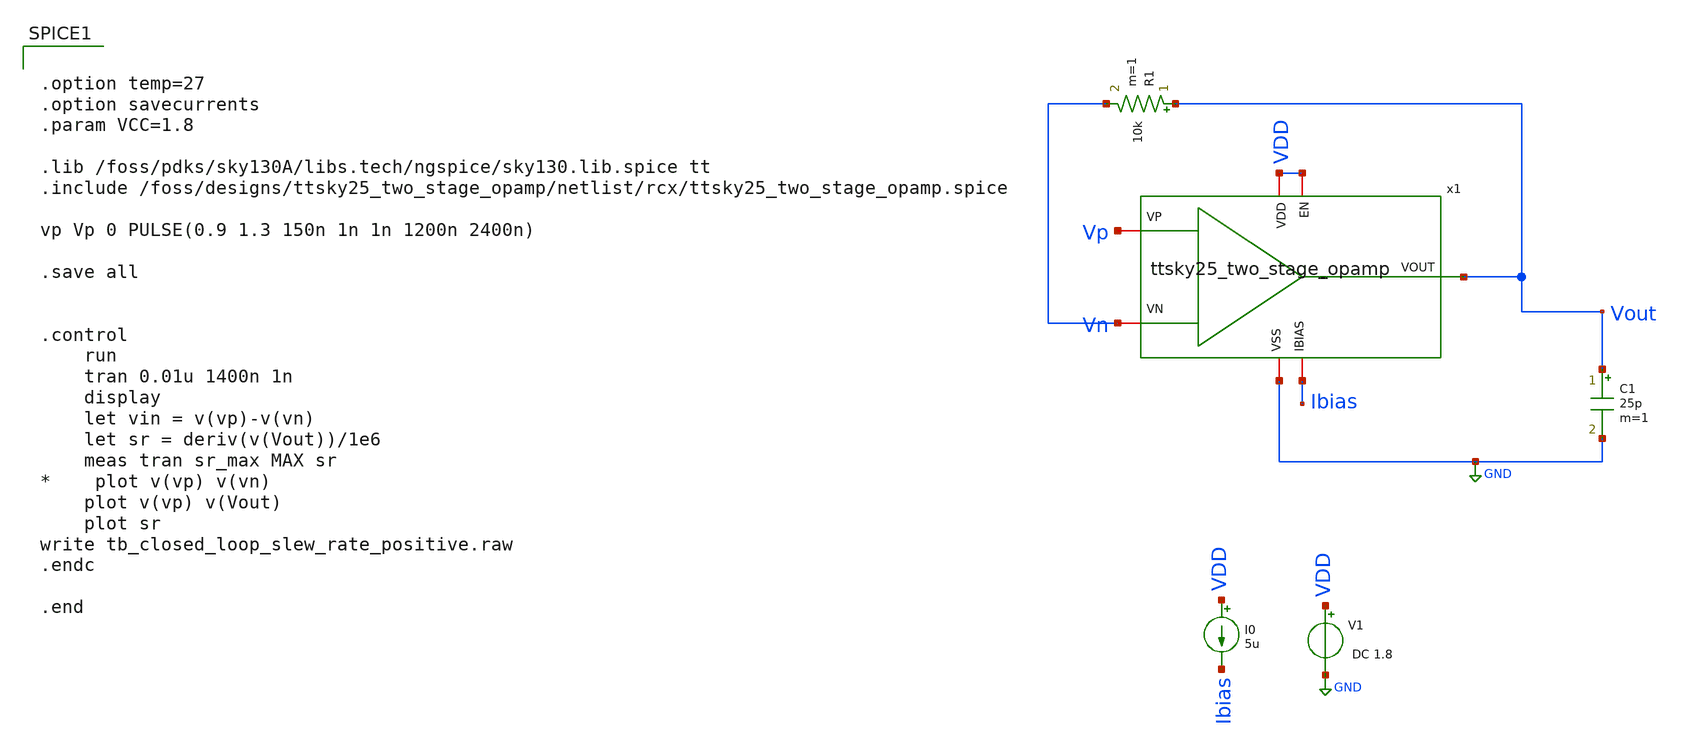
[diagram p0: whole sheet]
** sch_path: xschem/post-layout/testbenches/tb_closed_loop_slew_rate_positive.sch
**.subckt tb_closed_loop_slew_rate_positive
V1 VDD GND DC 1.8
I0 VDD Ibias 5u
C1 Vout GND 25p m=1
R1 Vout Vn 10k m=1
x1 VDD Ibias Vout Vn Vp VDD GND ttsky25_two_stage_opamp
**** begin user architecture code


.option temp=27
.option savecurrents
.param VCC=1.8

.lib /foss/pdks/sky130A/libs.tech/ngspice/sky130.lib.spice tt
.include /foss/designs/ttsky25_two_stage_opamp/netlist/rcx/ttsky25_two_stage_opamp.spice

vp Vp 0 PULSE(0.9 1.3 150n 1n 1n 1200n 2400n)

.save all


.control
	run
	tran 0.01u 1400n 1n
	display
	let vin = v(vp)-v(vn)
	let sr = deriv(v(Vout))/1e6
	meas tran sr_max MAX sr
*	plot v(vp) v(vn)
	plot v(vp) v(Vout)
	plot sr
write tb_closed_loop_slew_rate_positive.raw
.endc

.end


**** end user architecture code
**.ends
.GLOBAL GND
.end
